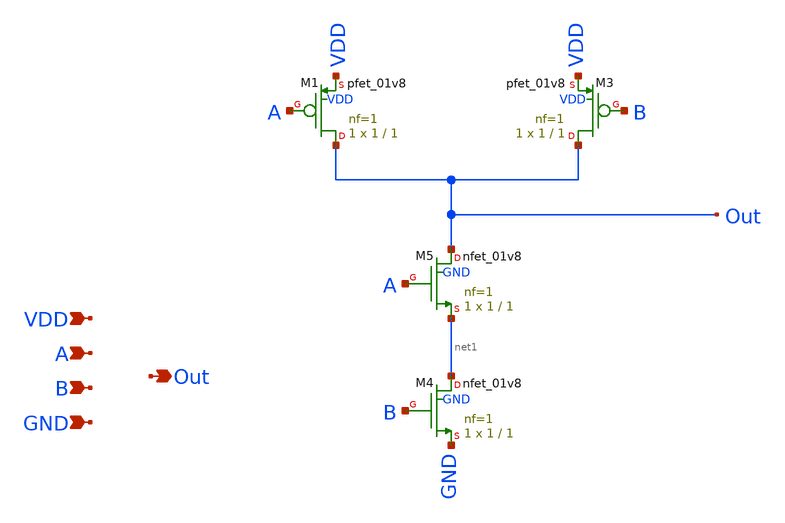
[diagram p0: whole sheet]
** sch_path: src/NAND2.sch
**.subckt NAND2 Out A B VDD GND
*.opin Out
*.ipin A
*.ipin B
*.ipin VDD
*.ipin GND
XM1 Out A VDD VDD sky130_fd_pr__pfet_01v8 L=1 W=1 nf=1 ad='int((1 + 1)/2) * 1 / 1 * 0.29' as='int((1 + 2)/2) * 1 / 1 * 0.29'
+ pd='2*int((1 + 1)/2) * (1 / 1 + 0.29)' ps='2*int((1 + 2)/2) * (1 / 1 + 0.29)' nrd='0.29 / 1 ' nrs='0.29 / 1 '
+ sa=0 sb=0 sd=0 mult=1 m=1
XM3 Out B VDD VDD sky130_fd_pr__pfet_01v8 L=1 W=1 nf=1 ad='int((1 + 1)/2) * 1 / 1 * 0.29' as='int((1 + 2)/2) * 1 / 1 * 0.29'
+ pd='2*int((1 + 1)/2) * (1 / 1 + 0.29)' ps='2*int((1 + 2)/2) * (1 / 1 + 0.29)' nrd='0.29 / 1 ' nrs='0.29 / 1 '
+ sa=0 sb=0 sd=0 mult=1 m=1
XM4 net1 B GND GND sky130_fd_pr__nfet_01v8 L=1 W=1 nf=1 ad='int((1 + 1)/2) * 1 / 1 * 0.29' as='int((1 + 2)/2) * 1 / 1 * 0.29'
+ pd='2*int((1 + 1)/2) * (1 / 1 + 0.29)' ps='2*int((1 + 2)/2) * (1 / 1 + 0.29)' nrd='0.29 / 1 ' nrs='0.29 / 1 '
+ sa=0 sb=0 sd=0 mult=1 m=1
XM5 Out A net1 GND sky130_fd_pr__nfet_01v8 L=1 W=1 nf=1 ad='int((1 + 1)/2) * 1 / 1 * 0.29' as='int((1 + 2)/2) * 1 / 1 * 0.29'
+ pd='2*int((1 + 1)/2) * (1 / 1 + 0.29)' ps='2*int((1 + 2)/2) * (1 / 1 + 0.29)' nrd='0.29 / 1 ' nrs='0.29 / 1 '
+ sa=0 sb=0 sd=0 mult=1 m=1
**** begin user architecture code

** opencircuitdesign pdks install
.lib $::SKYWATER_MODELS/sky130.lib.spice tt


**** end user architecture code
**.ends
.end
